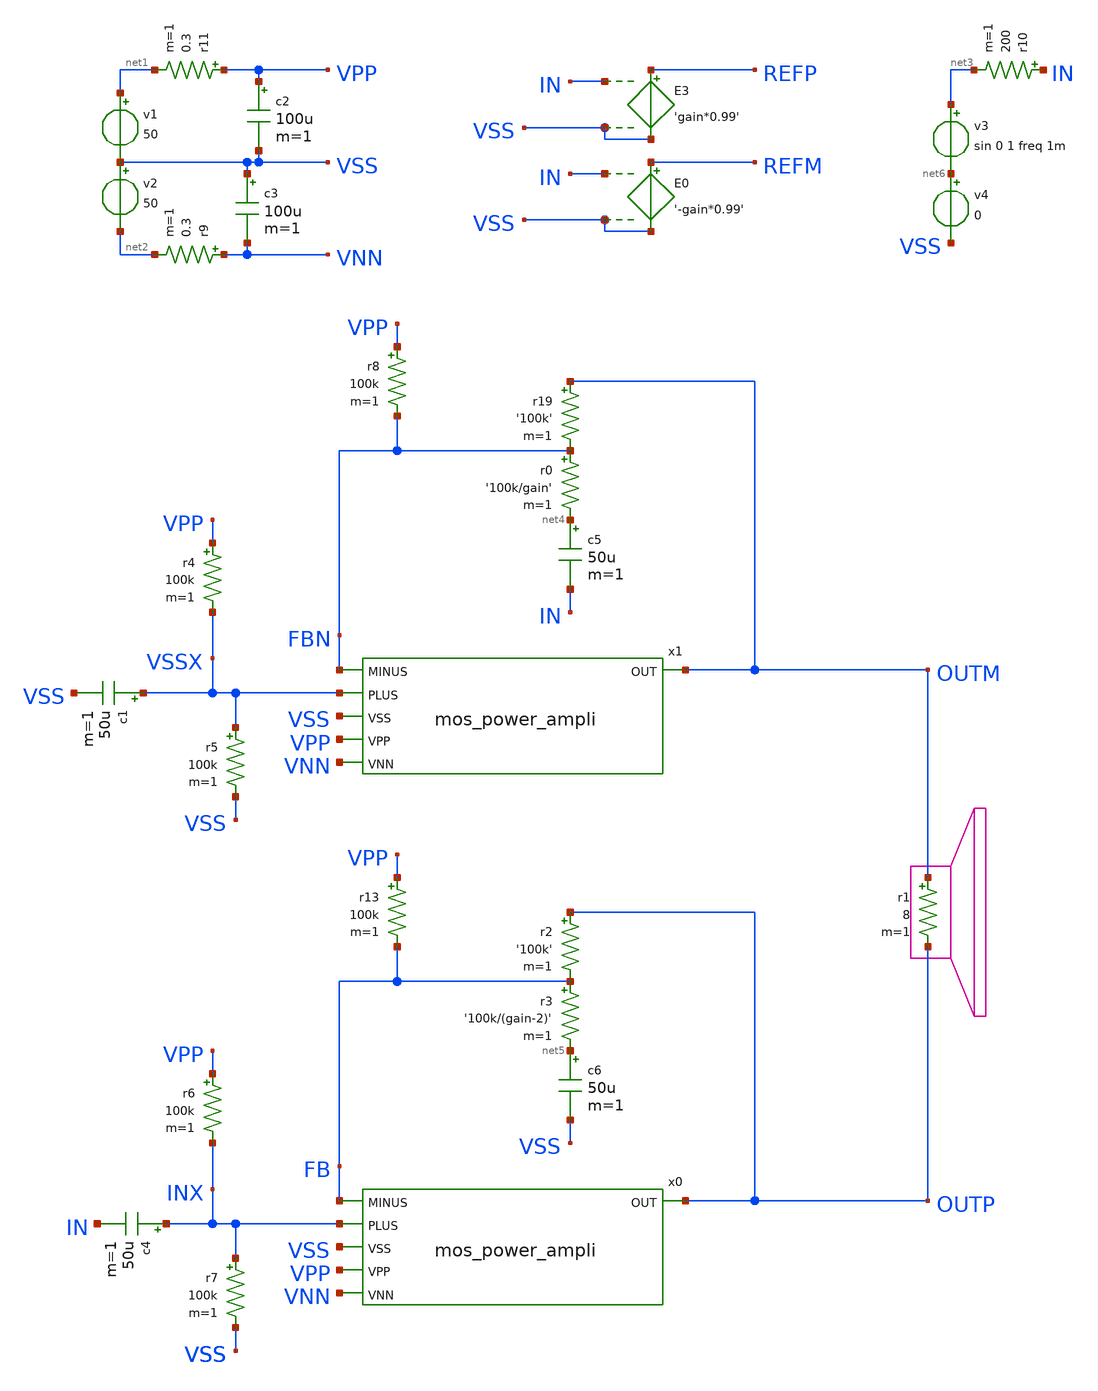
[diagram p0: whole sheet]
** sch_path: library/examples/poweramp.sch
**.subckt poweramp
** BJT MODELS : http://www.zen22142.zen.co.uk/ltspice/standard.bjt
** NPN MODELS : http://web.mit.edu/Magic/Public/ckt/npn.mod
** ltwiki BJT MODELS : http://ltwiki.org/?title=Standard.bjt
v1 net1 VSS 50
v2 VSS net2 50
r1 OUTM OUTP 8 m=1
E3 REFP VSS IN VSS 'gain*0.99'
c2 VPP VSS 100u m=1
c3 VSS VNN 100u m=1
r11 VPP net1 0.3 m=1
r9 VNN net2 0.3 m=1
r19 OUTM FBN '100k' m=1
r0 FBN net4 '100k/gain' m=1
x1 OUTM VSSX FBN VPP VNN VSS mos_power_ampli
x0 OUTP INX FB VPP VNN VSS mos_power_ampli
r6 VPP INX 100k m=1
r7 INX VSS 100k m=1
E0 REFM VSS IN VSS '-gain*0.99'
c5 net4 IN 50u m=1
c6 net5 VSS 50u m=1
r2 OUTP FB '100k' m=1
r3 FB net5 '100k/(gain-2)' m=1
v3 net3 net6 sin 0 1 freq 1m
r4 VPP VSSX 100k m=1
r5 VSSX VSS 100k m=1
r8 VPP FBN 100k m=1
c4 INX IN 50u m=1
c1 VSSX VSS 50u m=1
r10 IN net3 200 m=1
r13 VPP FB 100k m=1
** REGULATORS LIB : http://ltwiki.org/files/LTspiceIV/lib/sub/regulators.lib
v4 net6 VSS 0
** GENERATE NETLIST : www.google.com
**** begin user architecture code

.option PARHIER=LOCAL RUNLVL=6 post MODMONTE=1 warn maxwarns=400
.option sampling_method = SRS
.option method=gear
vvss vss 0 dc 0
.temp 30

.param freq=20k
.param gain=45
.tran '0.2m/freq' '3m + 80/freq'
.FOUR 20k v(outm,outp)
.probe i(*)
.probe p(r*) p(v*)


.MODEL bd139_2 npn IS=1e-09 BF=222.664 NF=0.85 VAF=36.4079 IKF=0.166126 ISE=5.03418e-09 NE=1.45313
+ BR=1.35467 NR=1.33751 VAR=142.931 IKR=1.66126 ISC=5.02557e-09 NC=3.10227 RB=26.9143 IRB=0.1 RBM=0.1
+ RE=0.000472454 RC=1.04109 XTB=0.727762 XTI=1.04311 EG=1.05 CJE=1e-11 VJE=0.75 MJE=0.33 TF=1e-09 XTF=1 VTF=10
+ ITF=0.01 CJC=1e-11 VJC=0.75 MJC=0.33 XCJC=0.9 FC=0.5 CJS=0 VJS=0.75 MJS=0.5 TR=1e-07 PTF=0 KF=0 AF=1


.MODEL BD139 NPN ( IS=2.3985E-13 Vceo=80 Icrating=1500m BF=244.9 NF=1.0 BR=78.11 NR=1.007
+ ISE=1.0471E-14 NE=1.2 ISC=1.9314E-11 NC=1.45 VAF=98.5 VAR=7.46 IKF=1.1863 IKR=0.1445 RB=2.14 RBM=0.001 IRB=0.031
+ RE=0.0832 RC=0.01 CJE=2.92702E-10 VJE=0.67412 MJE=0.3300 FC=0.5 CJC=4.8831E-11 VJC=0.5258 MJC=0.3928
+ XCJC=0.5287 XTB=1.1398 EG=1.2105 XTI=3.0)


.MODEL BD140  PNP(IS=1e-09 BF=650.842 NF=0.85 VAF=10 IKF=0.0950125 ISE=1e-08 NE=1.54571 BR=56.177
+ NR=1.5 VAR=2.11267 IKR=0.950125 ISC=1e-08 NC=3.58527 RB=41.7566 IRB=0.1 RBM=0.108893 RE=0.000347052
+ RC=1.32566 XTB=19.5239 XTI=1 EG=1.05 CJE=1e-11 VJE=0.75 MJE=0.33 TF=1e-09 XTF=1 VTF=10 ITF=0.01 CJC=1e-11
+ VJC=0.75 MJC=0.33 XCJC=0.9 FC=0.5 CJS=0 VJS=0.75 MJS=0.5 TR=1e-07 PTF=0 KF=0 AF=10  VCEO=80 ICRATING=1A )


.MODEL Q2N2222A NPN IS =3.0611E-14 NF =1.00124 BF =220 IKF=0.52                VAF=104 ISE=7.5E-15
+ NE =1.41 NR =1.005 BR =4 IKR=0.24                VAR=28 ISC=1.06525E-11 NC =1.3728 RB =0.13 RE =0.22
+                RC =0.12 CJC=9.12E-12 MJC=0.3508 VJC=0.4089                CJE=27.01E-12 TF =0.325E-9 TR =100E-9
+               vce_max=45 vbe_max=6

.MODEL Q2N2222 NPN (  IS = 3.97589E-14 BF = 195.3412 NF = 1.0040078 VAF = 53.081 IKF = 0.976 ISE =
+ 1.60241E-14  NE = 1.4791931 BR = 1.1107942 NR = 0.9928261 VAR = 11.3571702 IKR = 2.4993953 ISC = 1.88505E-12
+  NC = 1.1838278 RB = 56.5826472 IRB = 1.50459E-4 RBM = 5.2592283 RE = 0.0402974 RC = 0.4208  CJE =
+ 2.56E-11 VJE = 0.682256 MJE = 0.3358856 TF = 3.3E-10 XTF = 6 VTF = 0.574  ITF = 0.32 PTF = 25.832 CJC =
+ 1.40625E-11 VJC = 0.5417393 MJC = 0.4547893 XCJC = 1  TR = 3.2E-7 CJS = 0 VJS = .75 MJS = 0 XTB = 1.6486 EG =
+ 1.11  XTI = 5.8315 KF = 0 AF = 1 FC = 0.83               vce_max=45 vbe_max=6 )


* 2n2222 p complementary
.MODEL Q2N2907P PNP(IS=650.6E-18 ISE=54.81E-15 ISC=0 XTI=3  BF=231.7 BR=3.563 IKF=1.079 IKR=0
+ XTB=1.5  VAF=115.7 VAR=35 VJE=0.65 VJC=0.65  RE=0.15 RC=0.715 RB=10  CJE=19.82E-12 CJC=14.76E-12 XCJC=0.75
+ FC=0.5  NF=1 NR=1 NE=1.829 NC=2 MJE=0.3357 MJC=0.5383  TF=603.7E-12 TR=111.3E-9 ITF=0.65 VTF=5 XTF=1.7
+  EG=1.11 KF=1E-9 AF=1  VCEO=45 ICRATING=100M                vce_max=45 vbe_max=6 )

.MODEL Q2N2907S PNP(IS=2.32E-13 ISE=6.69E-16 ISC=1.65E-13 XTI=3.00  BF=3.08E2 BR=2.18E1 IKF=8.42E-1
+ IKR=1.00 XTB=1.5  VAF=1.41E2 VAR=1.35E1 VJE=3.49E-1 VJC=3.00E-1  RE=1.00E-2 RC=8.46E-1 RB=4.02E1 RBM=1.00E-2
+ IRB=1.25E-2  CJE=2.66E-11 CJC=1.93E-11 XCJC=1.00 FC=5.00E-1  NF=1.04 NR=1.12 NE=1.09 NC=1.13 MJE=4.60E-1
+ MJC=4.65E-1  TF=4.95E-10 TR=0 PTF=0 ITF=3.36E-1 VTF=6.54 XTF=1.87E1  EG=1.11 KF=1E-9 AF=1  VCEO=40
+ ICRATING=500M                vce_max=45 vbe_max=6 )

*MM3725 MCE 5/13/95
*Si    1W  40V 500mA 307MHz pkg:TO-39 3,2,1
.MODEL QMM3725 NPN (IS=50.7F NF=1 BF=162 VAF=113 IKF=.45 ISE=38.2P NE=2  BR=4 NR=1 VAR=24 IKR=.675
+ RE=.263 RB=1.05 RC=.105 XTB=1.5  CJE=62.2P VJE=1.1 MJE=.5 CJC=14.6P VJC=.3 MJC=.3 TF=518P TR=45.9N)

*MPS651 MCE 5/12/95
*Si 625mW  60V    2A 110MHz pkg:TO-92 1,2,3
.MODEL QMPS651 NPN (IS=72.1F NF=1 BF=260 VAF=139 IKF=2.5 ISE=67.1P NE=2  BR=4 NR=1 VAR=20 IKR=3.75
+ RE=28.2M RB=.113 RC=11.3M XTB=1.5  CJE=212P VJE=1.1 MJE=.5 CJC=68.6P VJC=.3 MJC=.3 TF=1.44N TR=1U)

*FCX649 ZETEX Spice model   Last revision  17/7/90   Medium Power
*ZTX Si  1.5W  25V    2A 240MHz pkg:SOT-89 2,1,3
.MODEL QFCX649 NPN(IS=3E-13 BF=225 VAF=80 IKF=2.8 ISE=1.1E-13 NE=1.37   BR=110 NR=0.972 VAR=28
+ IKR=0.8 ISC=6.5E-13 NC=1.372 RB=0.3 RE=0.063   RC=0.07 CJE=3.25E-10 TF=1E-9 CJC=7E-11 TR=1E-8 )

*MPSW01A MCE 5/12/95
*Si    1W  40V    1A 210MHz pkg:TO-92 1,2,3
.MODEL QMPSW01A NPN (IS=18.1F NF=1 BF=273 VAF=113 IKF=.6 ISE=15.7P NE=2  BR=4 NR=1 VAR=20 IKR=.9
+ RE=96.5M RB=.386 RC=38.6M XTB=1.5  CJE=78.7P VJE=1.1 MJE=.5 CJC=17.3P VJC=.3 MJC=.3 TF=757P TR=526N)

*BC546 ZETEX Spice model     Last revision  4/90   General Purpose
*ZTX Si 500mW  65V 200mA 300MHz pkg:TO-92 1,2,3
.MODEL BC546 NPN(IS=1.8E-14 BF=400 NF=0.9955 VAF=80 IKF=0.14 ISE=5E-14   NE=1.46 BR=35.5 NR=1.005
+ VAR=12.5 IKR=0.03 ISC=1.72E-13 NC=1.27 RB=0.56   RE=0.6 RC=0.25 CJE=1.3E-11 TF=6.4E-10 CJC=4E-12 VJC=0.54
+ TR=5.072E-8       vce_max=65 vbe_max=6 )


.MODEL BC556 PNP(       IS=2.059E-14      NF=1.003      ISE=2.971E-15      NE=1.316      BF=227.3
+      IKF=0.08719      VAF=37.2      NR=1.007      ISC=1.339E-14      NC=1.15      BR=7.69      IKR=0.07646
+      VAR=11.42      RB=1      IRB=1E-06      RBM=1      RE=0.688      RC=0.6437      XTB=0      EG=1.11      XTI=3
+      CJE=1.4E-11      VJE=0.5912      MJE=0.3572      TF=7.046E-10      XTF=4.217      VTF=5.367      ITF=0.1947
+      PTF=0      CJC=1.113E-11      VJC=0.1      MJC=0.3414      XCJC=0.6288      TR=1E-32      CJS=0
+      VJS=0.75      MJS=0.333      FC=0.7947      vce_max=65 vbe_max=6 )
*

* NXP Semiconductors
*
* Medium power NPN transistor
* IC   = 1 A
* VCEO = 20 V
* hFE  = 85 - 375 @ 2V/500mA
*
*
*
*
* Package pinning does not match Spice model pinning.
* Package: SOT 223
*
* Package Pin 1: Base
* Package Pin 2: Collector
* Package Pin 3: Emitter
* Package Pin 4: Collector
*
* Extraction date (week/year): 13/2008
* Simulator: Spice 3
*
**********************************************************
*#
.SUBCKT BCP68 1 2 3
*
Q1 1 2 3 BCP68
D1 2 1 DIODE
*
*The diode does not reflect a
*physical device but improves
*only modeling in the reverse
*mode of operation.
*
.MODEL BCP68 NPN   IS = 2.312E-013   NF = 0.988   ISE = 8.851E-014   NE = 2.191   BF = 273   IKF =
+ 5.5   VAF = 50   NR = 0.9885   ISC = 6.808E-014   NC = 3   BR = 155.6   IKR = 4   VAR = 17   RB = 15
+   IRB = 2E-006   RBM = 0.65   RE = 0.073   RC = 0.073   XTB = 0   EG = 1.11   XTI = 3   CJE = 2.678E-010
+   VJE = 0.732   MJE = 0.3484   TF = 5.8E-010   XTF = 1.5   VTF = 2.5   ITF = 1   PTF = 0   CJC =
+ 3.406E-011   VJC = 2   MJC = 0.3142   XCJC = 1   TR = 6.5E-009   CJS = 0   VJS = 0.75   MJS = 0.333   FC =
+ 0.95
.MODEL DIODE D   IS = 2.702E-015   N = 1.2   BV = 1000   IBV = 0.001   RS = 0.1   CJO = 0   VJ = 1
+   M = 0.5   FC = 0   TT = 0   EG = 1.11   XTI = 3
.ENDS

.model D1N4007 D(IS=7.02767n RS=0.0341512 N=1.80803 EG=1.05743 XTI=5 BV=1000 IBV=5e-08 CJO=1e-11
+ VJ=0.7 M=0.5 FC=0.5 TT=1e-07 )

.MODEL D1N4148 D   IS = 4.352E-9   N = 1.906   BV = 110   IBV = 0.0001   RS = 0.6458   CJO =
+ 7.048E-13   VJ = 0.869   M = 0.03   FC = 0.5   TT = 3.48E-9

.MODEL D1n5400 d IS=2.61339e-12 RS=0.0110501 N=1.20576 EG=0.6 XTI=3.1271 BV=50 IBV=1e-05 CJO=1e-11
+ VJ=0.7 M=0.5 FC=0.5 TT=1e-09 KF=0 AF=1
* Model generated on October 12, 2003
* Model format: PSpice

*1N758
*Ref: Motorola
*10V 500mW Si Zener pkg:DIODE0.4 1,2
.MODEL D1N758 D(IS=1E-11 RS=8.483 N=1.27 TT=5E-8 CJO=2.334E-10 VJ=0.75   M=0.33 BV=9.83 IBV=0.01 )

*1N4744
*Ref: Motorola
*15V 1W Si Zener pkg:DIODE0.4 1,2
.MODEL D1N4744 D(IS=5.32E-14 RS=6.47 TT=5.01E-8 CJO=7.83E-11 M=0.33   BV=14.89 IBV=0.017 )

*1N755
*Ref: Motorola
*7.5V 500mW Si Zener pkg:DIODE0.4 1,2
.MODEL D1N755 D(IS=1E-11 RS=3.359 N=1.27 TT=5E-8 CJO=2.959E-10 VJ=0.75   M=0.33 BV=7.433 IBV=0.01 )

** node order
* 1: gnd
* 2: trig
* 3: out
* 4: reset#
* 5: ctrl
* 6: thres
* 7: dis
* 8: vcc
.SUBCKT ne555  34 32 30 19 23 33 1  21
*              G  TR O  R  F  TH D  V
Q4 25 2 3 QP
Q5 34 6 3 QP
Q6 6 6 8 QP
R1 9 21 4.7K
R2 3 21 830
R3 8 21 4.7K
Q7 2 33 5 QN
Q8 2 5 17 QN
Q9 6 4 17 QN
Q10 6 23 4 QN
Q11 12 20 10 QP
R4 10 21 1K
Q12 22 11 12 QP
Q13 14 13 12 QP
Q14 34 32 11 QP
Q15 14 18 13 QP
R5 14 34 100K
R6 22 34 100K
R7 17 34 10K
Q16 1 15 34 QN
Q17 15 19 31 QP
R8 18 23 5K
R9 18 34 5K
R10 21 23 5K
Q18 27 20 21 QP
Q19 20 20 21 QP
R11 20 31 5K
D1 31 24 DA
Q20 24 25 34 QN
Q21 25 22 34 QN
Q22 27 24 34 QN
R12 25 27 4.7K
R13 21 29 6.8K
Q23 21 29 28 QN
Q24 29 27 16 QN
Q25 30 26 34 QN
Q26 21 28 30 QN
D2 30 29 DA
R14 16 15 100
R15 16 26 220
R16 16 34 4.7K
R17 28 30 3.9K
Q3 2 2 9 QP
.MODEL DA D (RS=40 IS=1.0E-14 CJO=1PF)
.MODEL QP PNP (level=1 BF=20 BR=0.02 RC=4 RB=25 IS=1.0E-14 VA=50 NE=2)  CJE=12.4P VJE=1.1 MJE=.5
+ CJC=4.02P VJC=.3 MJC=.3 TF=229P TR=159N)
.MODEL QN NPN (level=1 IS=5.07F NF=1 BF=100 VAF=161 IKF=30M ISE=3.9P NE=2  BR=4 NR=1 VAR=16 IKR=45M
+ RE=1.03 RB=4.12 RC=.412 XTB=1.5  CJE=12.4P VJE=1.1 MJE=.5 CJC=4.02P VJC=.3 MJC=.3 TF=229P TR=959P)
.ENDS

.SUBCKT BS250P 3 4 5
*              D G S
M1 3 2 5 5 MBS250
RG 4 2 160
RL 3 5 1.2E8
C1 2 5 47E-12
C2 3 2 10E-12
D1 3 5 DBS250
*
.MODEL MBS250 PMOS VTO=-3.193 RS=2.041 RD=0.697 IS=1E-15 KP=0.277 CBD=105E-12 PB=1 LAMBDA=1.2E-2
.MODEL DBS250 D IS=2E-13 RS=0.309
.ENDS BS250P

.SUBCKT BS170 3 4 5
*             D G S
M1 3 2 5 5 N3306M
RG 4 2 270
RL 3 5 1.2E8
C1 2 5 28E-12
C2 3 2 3E-12
D1 5 3 N3306D
*
.MODEL N3306M NMOS VTO=1.824 RS=1.572 RD=1.436 IS=1E-15 KP=.1233 CBD=35E-12 PB=1
.MODEL N3306D D IS=5E-12 RS=.768
.ENDS BS170
*

.SUBCKT irf540 1 2 3
**************************************
* Model Generated by MODPEX *
*Copyright(c) Symmetry Design Systems*
* All Rights Reserved *
* UNPUBLISHED LICENSED SOFTWARE *
* Contains Proprietary Information *
* Which is The Property of *
* SYMMETRY OR ITS LICENSORS *
*Commercial Use or Resale Restricted *
* by Symmetry License Agreement *
**************************************
* Model generated on Apr 24, 96
* Model format: SPICE3
* Symmetry POWER MOS Model (Version 1.0)
* External Node Designations
* Node 1 -> Drain
* Node 2 -> Gate
* Node 3 -> Source
M1 9 7 8 8 MM L=100u W=100u
* Default values used in MM:
* The voltage-dependent capacitances are
* not included. Other default values are:
* RS=0 RD=0 LD=0 CBD=0 CBS=0 CGBO=0
.MODEL MM NMOS LEVEL=1 IS=1e-32 VTO=3.56362 LAMBDA=0.00291031 KP=25.0081 CGSO=1.60584e-05
+ CGDO=4.25919e-07
RS 8 3 0.0317085
D1 3 1 MD
.MODEL MD D IS=1.02194e-10 RS=0.00968022 N=1.21527 BV=100 IBV=0.00025 EG=1.2 XTI=3.03885 TT=1e-07
+ CJO=1.81859e-09 VJ=1.1279 M=0.449161 FC=0.5
RDS 3 1 4e+06
RD 9 1 0.0135649
RG 2 7 5.11362
D2 4 5 MD1
* Default values used in MD1:
* RS=0 EG=1.11 XTI=3.0 TT=0
* BV=infinite IBV=1mA
.MODEL MD1 D IS=1e-32 N=50 CJO=2.49697e-09 VJ=0.5 M=0.9 FC=1e-08
D3 0 5 MD2
* Default values used in MD2:
* EG=1.11 XTI=3.0 TT=0 CJO=0
* BV=infinite IBV=1mA
.MODEL MD2 D IS=1e-10 N=0.4 RS=3e-06
RL 5 10 1
FI2 7 9 VFI2 -1
VFI2 4 0 0
EV16 10 0 9 7 1
CAP 11 10 2.49697e-09
FI1 7 9 VFI1 -1
VFI1 11 6 0
RCAP 6 10 1
D4 0 6 MD3
* Default values used in MD3:
* EG=1.11 XTI=3.0 TT=0 CJO=0
* RS=0 BV=infinite IBV=1mA
.MODEL MD3 D IS=1e-10 N=0.4
.ENDS




*$
*LM5134A
*****************************************************************************
* (C) Copyright 2016 Texas Instruments Incorporated. All rights reserved.
*****************************************************************************
** This model is designed as an aid for customers of Texas Instruments.
** TI and its licensors and suppliers make no warranties, either expressed
** or implied, with respect to this model, including the warranties of
** merchantability or fitness for a particular purpose.  The model is
** provided solely on an "as is" basis.  The entire risk as to its quality
** and performance is with the customer.
*****************************************************************************
*
** Released by: WEBENCH Design Center,Texas Instruments Inc.
* Part: LM5134A
* Date: 23SEP2016
* Model Type: TRANSIENT
* Simulator: PSPICE
* Simulator Version: 16.2.0.p001
* EVM Order Number: NA
* EVM User's Guide: NA
* Datasheet: SNVS808CMAY 2012REVISED FEBRURARY 2016
*
* Model Version: Final 1.00
*
*****************************************************************************
*
* Updates:
*
* Final 1.00
* Release to Web
*
*****************************************************************************
*
* Model Usage Notes:
*
* A. Features have been modelled
*	1. Output timing characteristics
*	2. Output tr & tf vs VDD & CL Capacitor
*	3. tD-ON, tPD-ON, tD-OFF & tPD-OFF vs VDD
*	4. Output peak current limit for VDD = 10V
*	5. Input threshold for VDD = 10V
*	6. VDD UVLO Logic at TA = 25°C
*
* B. Features haven't been modelled
*	1. Supply Current vs Supply Voltage
*	2. Supply Current vs Load capacitance
*	3. Frequency dependent plots
*	4. Temperature dependent characteristics
*
*****************************************************************************
.SUBCKT LM5134A VDD PILOT OUT IN INB VSS
E_E2         INB_INT 0 INB VSS 1
C_U3_C1         U3_N16789866 U3_N16789873  5p
X_U3_U5         VDD U3_N16789873 U3_N16790218 0 RVAR  RREF=1
C_U3_C3         OUT U3_N16789866  1p

* E_U3_E1         U3_N16790231 OUT vol=' V(MGATE, 0) > 0.5? 5: -5'
E_U3_E1         U3_N16790231 OUT pwl(1) MGATE 0 0.49 -5 0.51 5

X_U3_U6         U3_N24836 VSS U3_N31827 0 RVAR   RREF=1
R_U3_R1         U3_N16790231 U3_N16789866  20
M_U3_M2         U3_N24836 U3_N16789871 OUT OUT PMOS01
E_U3_E4         U3_N16790218 0 pwl(1) VDD_INT 0   0 0, 4.5 0.9, 10  0.09, 12.6 0.08
X_U3_U10         VSS OUT d_d1
R_U3_R2         U3_N16789868 U3_N16789871  20
C_U3_C2         U3_N24836 U3_N16789871  5p
X_U3_U9         OUT VDD d_d1
C_U3_C5         OUT VDD  10p
C_U3_C6         OUT U3_N16789871  10p
C_U3_C4         VSS OUT  10p
M_U3_M1         U3_N16789873 U3_N16789866 OUT OUT NMOS01
E_U3_E3         U3_N31827 0 pwl(1) VDD_INT 0      0 0, 4.5  0.26, 10  0.01, 12.6 0.01
E_U3_E2         OUT U3_N16789868 vol= 'V(MGATE, 0) > 0.5? -5: 5'
E_U4_ABM4         U4_N14683241 0 vol= 'V(U4_ON_INT) >=0.5?V(VDD_INT):0'
C_U4_C3         U4_N14683221 0  1n
V_U4_V6         U4_N155225261 0 80m
R_U4_R2         U4_N14683241 U4_N14683221  1
X_U4_U47         U4_N14683247 U4_N14683251 d_d1
E_U4_ABM5         U4_N14683301 0 vol= 'V(U4_ON_INT)<0.5? V(VDD_INT):0'
C_U4_C1         U4_N14683247 0  1n
X_U4_S1    U4_N14683159 0 U4_N14683247 0 PTON_TOFF_U4_S1
X_U4_U44         U4_ON_INT PGATE U4_N14683147 AND2_BASIC_GEN  VDD=1   VSS=0 VTHRESH=500E-3
X_U4_U43         U4_N14683247 PGATE BUF_BASIC_GEN VDD=1 VSS=0   VTHRESH=0.5
R_U4_R3         U4_N14683301 U4_N14683281  1
X_U4_U7         N18232068 U4_N15541612 INV_BASIC_GEN  VDD=1 VSS=0   VTHRESH=500E-3
G_U4_G1         U4_N14683251 U4_N14683247 pwl(1) U4_N14683221 0      0 0, 4.5 140m, 10 500m, 12.6
+ 600m
G_U4_G2         U4_N14683247 0 pwl(1) U4_N14683281 0      0 0, 4.5 70m, 10 800m, 12.6 900m
X_U4_U8         MGATE U4_N15541600 INV_BASIC_GEN  VDD=1 VSS=0   VTHRESH=500E-3
C_U4_C4         U4_N14683281 0  1n
X_U4_S2    U4_N14683147 0 U4_N14683251 U4_N14683247 PTON_TOFF_U4_S2
X_U4_U48         U4_N155225261 U4_N14683247 d_d1
X_U4_U45         U4_N15541600 U4_N15541612 U4_ON_INT AND2_BASIC_GEN    VDD=1 VSS=0 VTHRESH=500E-3
V_U4_V5         U4_N14683251 0 1V
X_U4_U46         PGATE U4_ON_INT U4_N14683159 NOR2_BASIC_GEN  VDD=1   VSS=0 VTHRESH=500E-3
E_E1         IN_INT 0 IN VSS 1
E_E3         VDD_INT 0 VDD VSS 1
C_U2_C1         U2_N14683247 0  1n
X_U2_U46         MGATE U2_ON_INT U2_N14683159 NOR2_BASIC_GEN  VDD=1   VSS=0 VTHRESH=500E-3
X_U2_U7         PGATE U2_N15532894 INV_BASIC_GEN  VDD=1 VSS=0   VTHRESH=500E-3
G_U2_G1         U2_N14683251 U2_N14683247 pwl(1)  U2_N14683221 0      0 0,  4.5 58m,  10 140m,  12.6
+ 230m

E_U2_ABM5         U2_N14683301 0 vol= 'V(U2_ON_INT) <0.5? V(VDD_INT):0'

X_U2_U43         U2_N14683247 MGATE BUF_BASIC_GEN VDD=1 VSS=0   VTHRESH=0.5
X_U2_U48         U2_N147032561 U2_N14683247 d_d1
V_U2_V6         U2_N147032561 0 80m
X_U2_S2    U2_N14683147 0 U2_N14683251 U2_N14683247 MTON_TOFF_U2_S2

E_U2_ABM4         U2_N14683241 0 vol='V(U2_ON_INT) >=0.5? V(VDD_INT):0  '

R_U2_R2         U2_N14683241 U2_N14683221  1
G_U2_G2         U2_N14683247 0 PWL(1) U2_N14683281 0      0 0, 4.5 32m, 10 90m, 12.6 160m
V_U2_V5         U2_N14683251 0 1V
X_U2_U44         U2_ON_INT MGATE U2_N14683147 AND2_BASIC_GEN  VDD=1   VSS=0 VTHRESH=500E-3
C_U2_C3         U2_N14683221 0  1n
X_U2_U45         N18232068 U2_N15532894 U2_ON_INT AND2_BASIC_GEN  VDD=1   VSS=0 VTHRESH=500E-3
X_U2_S1    U2_N14683159 0 U2_N14683247 0 MTON_TOFF_U2_S1
R_U2_R3         U2_N14683301 U2_N14683281  1
C_U2_C4         U2_N14683281 0  1n
X_U2_U47         U2_N14683247 U2_N14683251 d_d1
X_U1_U6         INB_INT U1_VIH U1_VHYS U1_N15517298 COMPHYS_BASIC_GEN    VDD=1 VSS=0 VTHRESH=0.5
R_U1_R1         U1_N15521766 U1_VDD_UVLO  721.5
X_U1_U7         U1_N15517298 U1_INB_OUT INV_BASIC_GEN  VDD=1 VSS=0   VTHRESH=500E-3
X_U1_U9         U1_IN_OUT U1_INB_OUT U1_VDD_UVLO N18232068 AND3_BASIC_GEN    VDD=1 VSS=0
+ VTHRESH=500E-3
C_U1_C1         U1_VDD_UVLO 0  1n
X_U1_U5         IN_INT U1_VIH U1_VHYS U1_IN_OUT COMPHYS_BASIC_GEN  VDD=1   VSS=0 VTHRESH=0.5
X_U1_U8         VDD_INT U1_N15521824 U1_N15521760 U1_N15521766   COMPHYS_BASIC_GEN  VDD=1 VSS=0
+ VTHRESH=0.5
V_U1_V1         U1_N15521824 0 3.6
E_U1_ABM3         U1_VHYS 0 vol= '0.34*V(VDD_INT)'
E_U1_ABM1         U1_VIH 0 vol='0.67*V(VDD_INT)'
V_U1_V2         U1_N15521760 0 0.36
X_U1_U35         U1_VDD_UVLO U1_N15521766 d_d1
M_U5_M2         U5_N16789896 U5_N23038 PILOT PILOT PMOS02
R_U5_R1         U5_N16790231 U5_N16789866  20
X_U5_U6         U5_N16789896 VSS U5_N16802670 0 RVAR  RREF=1
M_U5_M1         U5_N08221 U5_N16789866 PILOT PILOT NMOS02
C_U5_C4         VSS PILOT  10p
C_U5_C2         U5_N16789896 U5_N23038  5p
R_U5_R2         U5_N16789868 U5_N23038  20
E_U5_E3         U5_N16802670 0 pwl(1) VDD_INT 0      0 0, 4.5 2.8, 10 1.9, 12.6 1.6
X_U5_U5         VDD U5_N08221 U5_N26349 0 RVAR RREF=1
C_U5_C1         U5_N08221 U5_N16789866  5p
C_U5_C5         PILOT VDD  10p
E_U5_E4         U5_N26349 0 pwl(1) VDD_INT 0      0 0, 4.5 9.5, 10 2.88, 12.6 2.8
X_U5_U9         PILOT VDD d_d1
C_U5_C3         PILOT U5_N16789866  10p
X_U5_U10         VSS PILOT d_d1
E_U5_E2         PILOT U5_N16789868 vol= ' V(PGATE, 0) > 0.5? -5: 5'
E_U5_E1         U5_N16790231 PILOT vol= ' V(PGATE, 0) > 0.5? 5: -5'
C_U5_C6         PILOT U5_N23038  10p
.ENDS LM5134A
*$
.SUBCKT PTON_TOFF_U4_S1 1 2 3 4
G_Switch 3 4 VCR PWL(1) 1 2 0.2 100e6 0.8 1m
RS_U4_S1         1 2 1G
.ENDS PTON_TOFF_U4_S1
*$
.SUBCKT PTON_TOFF_U4_S2 1 2 3 4
G_Switch 3 4 VCR PWL(1) 1 2 0.2 100e6 0.8 1m
RS_U4_S2         1 2 1G
.ENDS PTON_TOFF_U4_S2
*$
.SUBCKT MTON_TOFF_U2_S2 1 2 3 4
G_Switch 3 4 VCR PWL(1) 1 2 0.2 100e6 0.8 1m
RS_U2_S2         1 2 1G
.ENDS MTON_TOFF_U2_S2
*$
.SUBCKT MTON_TOFF_U2_S1 1 2 3 4
G_Switch 3 4 VCR PWL(1) 1 2 0.2 100e6 0.8 1m
RS_U2_S1         1 2 1G
.ENDS MTON_TOFF_U2_S1
*$
****************************** Basic Components **************************
.SUBCKT D_D1 1 2
D1 1 2 DD1
.MODEL DD1 D (IS=1e-15 Rs=0.001 N=0.1  TT=10p)
.ENDS D_D1
*$
.SUBCKT BUF_BASIC_GEN A  Y VDD=1 VSS=0 VTHRESH=0.5
* E_ABMGATE    YINT 0 vol='V(A) > VTHRESH? VDD:VSS'
E_ABMGATE    YINT 0 pwl(1) A 0 'VTHRESH-0.01' VSS 'VTHRESH+0.01' VDD
RINT YINT Y 1
CINT Y 0 1n
.ENDS BUF_BASIC_GEN
*$
.MODEL NMOS01 NMOS (VTO = 2 KP = 1.005 LAMBDA  = 0.001)
*$
.MODEL PMOS01 PMOS (VTO = -2 KP = 1.77 LAMBDA  = 0.001)
*$
.MODEL NMOS02 NMOS (VTO = 2 KP = 0.1814 LAMBDA = 0.001)
*$
.MODEL PMOS02 PMOS (VTO = -2 KP = 0.2497 LAMBDA = 0.001)
*$
.SUBCKT COMPHYS_BASIC_GEN INP INM HYS OUT VDD=1 VSS=0 VTHRESH=0.5
EIN INP1 INM1 INP INM 1
* EHYS INP1 INP2 vol='V(1) > VTHRESH? -V(HYS):0'
EHYS INP1 INP2 pwl(1) 1 0 'VTHRESH-0.01' 0 'VTHRESH+0.01' '-V(HYS)'

EOUT OUT 0 vol='V(INP2)>V(INM1)? VDD : VSS'
R1 OUT 1 1
C1 1 0 5n
RINP1 INP1 0 1K
.ENDS COMPHYS_BASIC_GEN
*$
.SUBCKT AND2_BASIC_GEN A B Y  VDD=1 VSS=0 VTHRESH=0.5
E_ABMGATE    YINT 0 vol= 'V(A) > VTHRESH  && V(B) > VTHRESH ? VDD:VSS'
RINT YINT Y 1
CINT Y 0 1n
.ENDS AND2_BASIC_GEN
*$
.SUBCKT NOR2_BASIC_GEN A B Y  VDD=1 VSS=0 VTHRESH=0.5
E_ABMGATE    YINT 0 vol= 'V(A) > VTHRESH  || V(B) > VTHRESH ? VSS:VDD'
RINT YINT Y 1
CINT Y 0 1n
.ENDS NOR2_BASIC_GEN
*$
.SUBCKT AND3_BASIC_GEN A B C Y VDD=1 VSS=0 VTHRESH=0.5
E_ABMGATE    YINT 0 vol= 'V(A) > VTHRESH  &&  V(B) > VTHRESH && V(C) > VTHRESH ? VDD:VSS'
RINT YINT Y 1
CINT Y 0 1n
.ENDS AND3_BASIC_GEN
*$
.SUBCKT INV_BASIC_GEN A  Y VDD=1 VSS=0 VTHRESH=0.5
* E_ABMGATE    YINT 0 vol='V(A) > VTHRESH ? VSS : VDD'
E_ABMGATE    YINT 0 pwl(1) A 0 'VTHRESH-0.01' VDD 'VTHRESH+0.01' VSS
RINT YINT Y 1
CINT Y 0 1n
.ENDS INV_BASIC_GEN
*$
.SUBCKT RVAR 101 102 201 202 RREF=1
* nodes : 101 102 : nodes between which variable resistance is placed
* 201 202 : nodes to whose voltage the resistance is proportional
* parameters : rref : reference value of the resistance
rin 201 202 1G   $$ input resistance
r 301 0 rref
fcopy 0 301 vsense 1 $$  copy output current thru Z
eout 101 106 poly(2) 201 202 301 0 0 0 0 0 1   $$ multiply VoverZ with Vctrl
vsense 106 102 0   $$ sense iout
.ENDS RVAR
*$


*LM317 TI voltage regulator - pin order: In, Adj, Out
*TI adjustable voltage regulator pkg:TO-3
.SUBCKT LM317 1 2 3 **Changes my be required on this line**
J1 1 3 4 JN
Q2 5 5 6 QPL .1
Q3 5 8 9 QNL .2
Q4 8 5 7 QPL .1
Q5 81 8 3 QNL .2
Q6 3 81 10 QPL .2
Q7 12 81 13 QNL .2
Q8 10 5 11 QPL .2
Q9 14 12 10 QPL .2
Q10 16 5 17 QPL .2
Q11 16 14 15 QNL .2
Q12 3 20 16 QPL .2
Q13 1 19 20 QNL .2
Q14 19 5 18 QPL .2
Q15 3 21 19 QPL .2
Q16 21 22 16 QPL .2
Q17 21 3 24 QNL .2
Q18 22 22 16 QPL .2
Q19 22 3 241 QNL 2
Q20 3 25 16 QPL .2
Q21 25 26 3 QNL .2
Q22A 35 35 1 QPL 2
Q22B 16 35 1 QPL 2
Q23 35 16 30 QNL 2
Q24A 27 40 29 QNL .2
Q24B 27 40 28 QNL .2
Q25 1 31 41 QNL 5
Q26 1 41 32 QNL 50
D1 3 4 DZ
D2 33 1 DZ
D3 29 34 DZ
R1 1 6 310
R2 1 7 310
R3 1 11 190
R4 1 17 82
R5 1 18 5.6K
R6 4 8 100K
R7 8 81 130
R8 10 12 12.4K
R9 9 3 180
R10 13 3 4.1K
R11 14 3 5.8K
R12 15 3 72
R13 20 3 5.1K
R14 2 24 12K
R15 24 241 2.4K
R16 16 25 6.7K
R17 16 40 12K
R18 30 41 130
R19 16 31 370
R20 26 27 13K
R21 27 40 400
R22 3 41 160
R23 33 34 18K
R24 28 29 160
R25 28 32 3
R26 32 3 .1
C1 21 3 30PF
C2 21 2 30PF
C3 25 26 5PF
CBS1 5 3 2PF
CBS2 35 3 1PF
CBS3 22 3 1PF
.MODEL JN NJF(BETA=1E-4 VTO=-7)
.MODEL DZ D(BV=6.3)
.MODEL QNL NPN(EG=1.22 BF=80 RB=100 CCS=1.5PF TF=.3NS TR=6NS CJE=2PF  CJC=1PF VAF=100)
.MODEL QPL PNP(BF=40 RB=20 TF=.6NS TR=10NS CJE=1.5PF CJC=1PF VAF=50)
.ENDS

.SUBCKT xxxxLM317 1 3 2
* IN ADJ OUT
IADJ 1 4 50U
VREF 4 3 1.25
RC 1 14 0.742
DBK 14 13 D1
CBC 13 15 2.479N
RBC 15 5 247
QP 13 5 2 Q1
RB2 6 5 124
DSC 6 11 D1
ESC 11 2 POLY(2) (13,5) (6,5) 2.85  0 0 0 -70.1M
DFB 6 12 D1
EFB 12 2 POLY(2) (13,5) (6,5) 3.92  -135M 0 1.21M -70.1M
RB1 7 6 1
EB 7 2 8 2 2.56
CPZ 10 2 0.796U
DPU 10 2 D1
RZ 8 10 0.104
RP 9 8 100
EP 9 2 4 2 103.6
RI 2 4 100MEG
.MODEL Q1 NPN (IS=30F BF=100  VAF=14.27 NF=1.604)
.MODEL D1 D (IS=30F N=1.604)
.ENDS



.SUBCKT LM337 8 1 19
*Connections Input Adj. Output
*LM337 negative voltage regulator
.MODEL QN NPN (BF=50 TF=1N CJC=1P)
.MODEL QPOUT PNP (BF=50 TF=1N RE=.2 CJC=1P)
.MODEL QP PNP CJC=1P TF=2N
.MODEL DN D
.MODEL D2 D BV=12 IBV=100U
R10 25 6 1K
Q3 8 17 16 QPOUT
Q4 8 25 17 QP
R18 19 17 250
R19 19 16 .3
G1 8 6 1 18 .1
C7 6 2 .04U
R24 2 8 100
I_ADJ 0 1 65U
R26 8 25 200K
Q5 25 4 19 QP
R27 16 4 200
R28 7 4 7K
D1 8 7 D2
D2 8 6 DN
V1 18 19 1.25
.ENDS

**** end user architecture code
**.ends

* expanding   symbol:  examples/mos_power_ampli.sym # of pins=6
** sym_path: xschem_library/examples/mos_power_ampli.sym
** sch_path: xschem_library/examples/mos_power_ampli.sch
.subckt mos_power_ampli OUT PLUS MINUS VPP VNN VSS
*.ipin PLUS
*.ipin VPP
*.ipin VNN
*.opin OUT
*.ipin MINUS
*.ipin VSS
*.ipin MINUS
xm2 net2 GB SB irf540 m=1
R7 GB SB 190 m=1
xm1 VPP GA SA irf540 m=1
R0 GA SA 190 m=1
R2 VPP E2 50 m=1
R3 VBOOST E1 50 m=1
Q5 C5 PLUS E9 q2n2222 area=1 m=1
Q4 net9 net3 E4 q2n2907p area=1 m=1
R9 VBOOST E4 50 m=1
Q6 C6 C2 net6 q2n2907p area=1 m=1
R4 VPP E6 50 m=1
vd net1 net2 0
.save i(vd)
vu SA net1 0
.save i(vu)
Q1 net3 net3 E1 q2n2907p area=1 m=1
Q2 C2 C2 net5 q2n2907p area=1 m=1
Q9 C9 MINUS E9 q2n2222 area=1 m=1
R11 GB net7 1300 m=1
Q8 C8 VSS E8 q2n2907p area=1 m=1
C12 VBOOST net4 40u m=1
D0 VPP VBOOST d1n4148 area=1
R18 net4 net1 200 m=1
D1 VPP VBOOST d1n758
R14 B1 net8 4k m=1
Q11 GA B1 E11 q2n2907p area=1 m=1
R15 VBOOST B1 4k m=1
R5 E9 net10 600 m=1
R6 net10 net11 700 m=1
D2 VNN B3 d1n755
Q3 C3 B3 E3 q2n2222 area=1 m=1
R1 VSS B3 10k m=1
R10 E3 VNN 170 m=1
C3 B3 VNN 100n m=1
R12 C6 E8 1300 m=1
R13 C2 C9 300 m=1
Q7 C7 C9 C5 q2n2222 area=1 m=1
v0 SB VNN 0
.save i(v0)
v1 E6 net6 0
.save i(v1)
v2 E2 net5 0
.save i(v2)
v3 net11 C3 0
.save i(v3)
v4 C8 net7 0
.save i(v4)
v5 net8 net1 0
.save i(v5)
v6 net3 C7 0
.save i(v6)
v7 net9 E11 0
.save i(v7)
.save v(gb)
.save v(gb)
.save v(sb)
.save v(ga)
.save v(sa)
.save v(ga)
.save v(net1)
.save v(minus)
.save v(plus)
.save v(e9)
.save v(c2)
.save v(net3)
.save v(b1)
.save v(vpp)
.save v(vboost)
v8 net1 OUT 0
.save i(v8)
.save v(vnn)
.save v(c9)
.save v(net5)
.save v(b3)
.save v(vnn)
**** begin user architecture code

.probe v(ga,sa) v(gb,sb)
.probe p(q*) p(r*) i(r*) p(xm1) p(xm2) i(d*)
**** end user architecture code
.ends

.end
